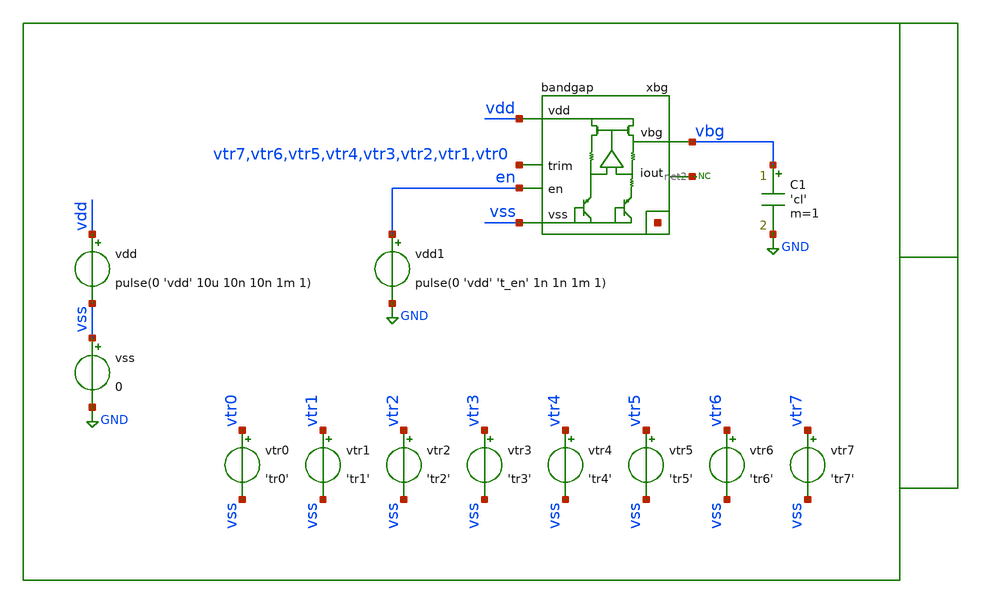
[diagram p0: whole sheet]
** sch_path: xschem/tb/bandgap_cm/bandgap/tr_bandgap_trim_ss.sch
* GPLv3
**.subckt tr_bandgap_trim_ss
xbg vdd vbg vss net1[7] net1[6] net1[5] net1[4] net1[3] net1[2] net1[1] net1[0] vtr7 vtr6 vtr5 vtr4
+ vtr3 vtr2 vtr1 vtr0 net2 en bandgap
vss vss GND 0
C1 vbg GND 'cl' m=1
vdd vdd vss pulse(0 'vdd' 10u 10n 10n 1m 1)
* noconn #net2
vdd1 en GND pulse(0 'vdd' 't_en' 1n 1n 1m 1)
vtr0 vtr0 vss 'tr0'
vtr1 vtr1 vss 'tr1'
vtr2 vtr2 vss 'tr2'
vtr3 vtr3 vss 'tr3'
vtr4 vtr4 vss 'tr4'
vtr5 vtr5 vss 'tr5'
vtr6 vtr6 vss 'tr6'
vtr7 vtr7 vss 'tr7'
**** begin user architecture code

* Control

.options reltol = 1e-6

.param vdd  = 3.3
.param cl   = 100e-15
.param t_en = 20u

.param tr0 = 0
.param tr1 = 0
.param tr2 = 0
.param tr3 = 0
.param tr4 = 0
.param tr5 = 0
.param tr6 = 0
.param tr7 = 0

.temp 27


.control
save all
tran 1u 200u

meas tran vbg_avg avg v(vbg) from=150e-6 to=199e-6

print vbg_avg

.endc
.end


 * Model Corners

.include $::CORNERS/ngspice/tt.spice
*.include $::CORNERS/ngspice/ff.spice
*.include $::CORNERS/ngspice/ss.spice
*.include $::CORNERS/ngspice/sf.spice
*.include $::CORNERS/ngspice/fs.spice

 * extract

* tb_amplifier pex
*.include $::DESIGN_PATH/sch/bandgap_cm/bg_amplifier/bg_amplifier.pex.spice

* bandgap pex
*.include $::DESIGN_PATH/sch/bandgap_cm/bandgap/bandgap.pex.spice

**** end user architecture code
**.ends
.GLOBAL GND
.end
